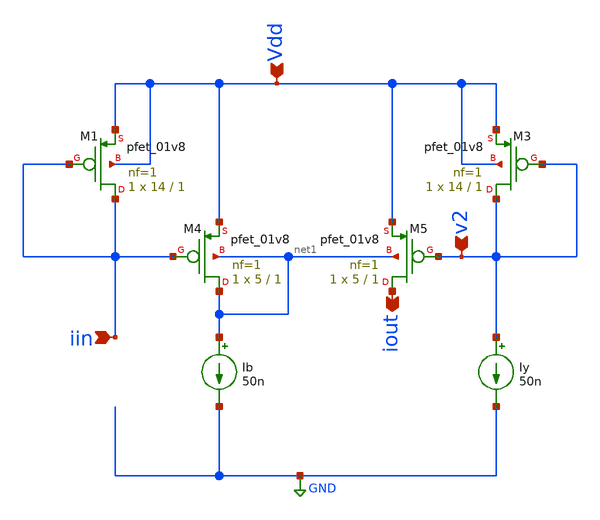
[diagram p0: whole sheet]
** sch_path: verified/0003_div.sch
**.subckt 0003_div Vdd v2 iout iin
*.ipin Vdd
*.ipin v2
*.opin iout
*.ipin iin
XM1 iin iin Vdd Vdd sky130_fd_pr__pfet_01v8 L=1 W=14 nf=1 ad='int((nf+1)/2) * W/nf * 0.29' as='int((nf+2)/2) * W/nf * 0.29'
+ pd='2*int((nf+1)/2) * (W/nf + 0.29)' ps='2*int((nf+2)/2) * (W/nf + 0.29)' nrd='0.29 / W' nrs='0.29 / W'
+ sa=0 sb=0 sd=0 mult=1 m=1
Ib net1 GND 50n
XM3 v2 v2 Vdd Vdd sky130_fd_pr__pfet_01v8 L=1 W=14 nf=1 ad='int((nf+1)/2) * W/nf * 0.29' as='int((nf+2)/2) * W/nf * 0.29'
+ pd='2*int((nf+1)/2) * (W/nf + 0.29)' ps='2*int((nf+2)/2) * (W/nf + 0.29)' nrd='0.29 / W' nrs='0.29 / W'
+ sa=0 sb=0 sd=0 mult=1 m=1
XM4 net1 iin Vdd net1 sky130_fd_pr__pfet_01v8 L=1 W=5 nf=1 ad='int((nf+1)/2) * W/nf * 0.29' as='int((nf+2)/2) * W/nf * 0.29'
+ pd='2*int((nf+1)/2) * (W/nf + 0.29)' ps='2*int((nf+2)/2) * (W/nf + 0.29)' nrd='0.29 / W' nrs='0.29 / W'
+ sa=0 sb=0 sd=0 mult=1 m=1
XM5 iout v2 Vdd net1 sky130_fd_pr__pfet_01v8 L=1 W=5 nf=1 ad='int((nf+1)/2) * W/nf * 0.29' as='int((nf+2)/2) * W/nf * 0.29'
+ pd='2*int((nf+1)/2) * (W/nf + 0.29)' ps='2*int((nf+2)/2) * (W/nf + 0.29)' nrd='0.29 / W' nrs='0.29 / W'
+ sa=0 sb=0 sd=0 mult=1 m=1
Iy v2 GND 50n
**.ends
.GLOBAL GND
.end
